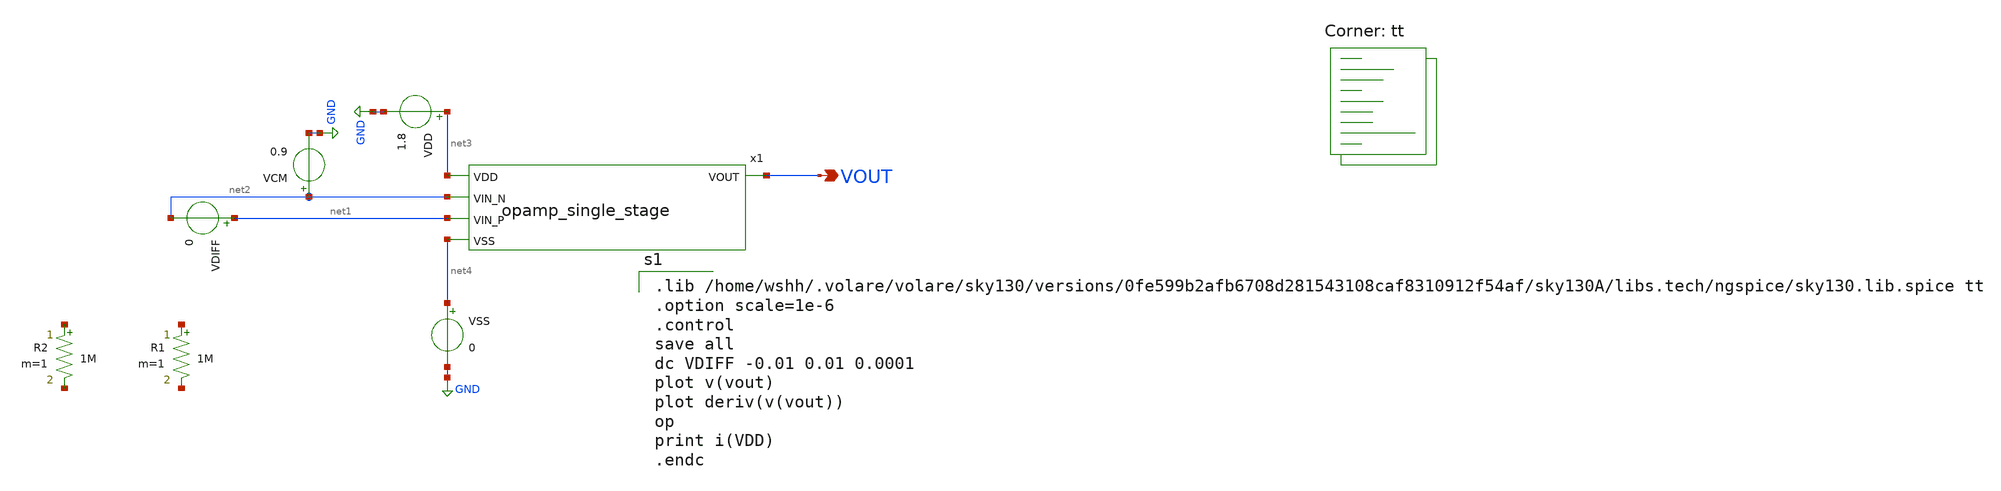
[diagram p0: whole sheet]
** sch_path: analog/build/schematic/tb_dc_analysis.sch
**.subckt tb_dc_analysis VOUT
*.opin VOUT
VSS net4 GND 0
VDD net3 GND 1.8
VCM net2 GND 0.9
VDIFF net1 net2 0
x1 net3 VOUT net2 net1 net4 opamp_single_stage
R1 net5 net6 1M m=1
R2 net7 net8 1M m=1
**** begin user architecture code

.lib /home/wshh/.volare/volare/sky130/versions/0fe599b2afb6708d281543108caf8310912f54af/sky130A/libs.tech/ngspice/sky130.lib.spice tt
.option scale=1e-6
.control
save all
dc VDIFF -0.01 0.01 0.0001
plot v(vout)
plot deriv(v(vout))
op
print i(VDD)
.endc


.lib $::SKYWATER_MODELS/sky130.lib.spice tt
**** end user architecture code
**.ends

* expanding   symbol:  /home/wshh/Shiheng_Analog_Bootcamp/analog/schematics/opamp_single_stage.sym #
*+ of pins=5
** sym_path: analog/schematics/opamp_single_stage.sym
** sch_path: analog/schematics/opamp_single_stage.sch
.subckt opamp_single_stage VDD VOUT VIN_N VIN_P VSS
*.ipin VIN_P
*.ipin VIN_N
*.ipin VDD
*.ipin VSS
*.opin VOUT
XM3 VDD net1 net1 VDD sky130_fd_pr__pfet_01v8 L=0.5 W=5 nf=1 ad='int((nf+1)/2) * W/nf * 0.29' as='int((nf+2)/2) * W/nf * 0.29'
+ pd='2*int((nf+1)/2) * (W/nf + 0.29)' ps='2*int((nf+2)/2) * (W/nf + 0.29)' nrd='0.29 / W' nrs='0.29 / W'
+ sa=0 sb=0 sd=0 mult=1 m=1
XM4 VOUT net1 VDD VDD sky130_fd_pr__pfet_01v8 L=0.5 W=5 nf=1 ad='int((nf+1)/2) * W/nf * 0.29' as='int((nf+2)/2) * W/nf * 0.29'
+ pd='2*int((nf+1)/2) * (W/nf + 0.29)' ps='2*int((nf+2)/2) * (W/nf + 0.29)' nrd='0.29 / W' nrs='0.29 / W'
+ sa=0 sb=0 sd=0 mult=1 m=1
VB2 net3 net4 0.7
XM9 net2 net3 VSS GND sky130_fd_pr__nfet_01v8 L=0.15 W=1 nf=1 ad='int((nf+1)/2) * W/nf * 0.29' as='int((nf+2)/2) * W/nf * 0.29'
+ pd='2*int((nf+1)/2) * (W/nf + 0.29)' ps='2*int((nf+2)/2) * (W/nf + 0.29)' nrd='0.29 / W' nrs='0.29 / W'
+ sa=0 sb=0 sd=0 mult=1 m=1
XM1 net1 VIN_P net2 GND sky130_fd_pr__nfet_01v8 L=0.5 W=5 nf=1 ad='int((nf+1)/2) * W/nf * 0.29' as='int((nf+2)/2) * W/nf * 0.29'
+ pd='2*int((nf+1)/2) * (W/nf + 0.29)' ps='2*int((nf+2)/2) * (W/nf + 0.29)' nrd='0.29 / W' nrs='0.29 / W'
+ sa=0 sb=0 sd=0 mult=1 m=1
XM2 net2 VIN_N VOUT GND sky130_fd_pr__nfet_01v8 L=0.5 W=5 nf=1 ad='int((nf+1)/2) * W/nf * 0.29' as='int((nf+2)/2) * W/nf * 0.29'
+ pd='2*int((nf+1)/2) * (W/nf + 0.29)' ps='2*int((nf+2)/2) * (W/nf + 0.29)' nrd='0.29 / W' nrs='0.29 / W'
+ sa=0 sb=0 sd=0 mult=1 m=1
.ends

.GLOBAL GND
.end
